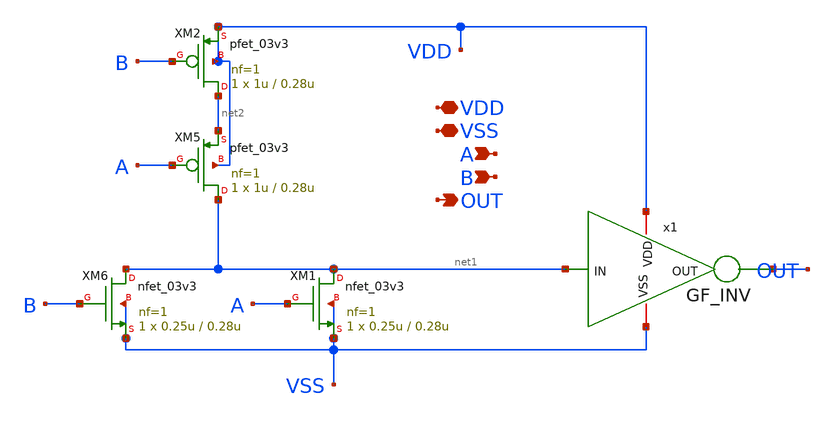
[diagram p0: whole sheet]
** sch_path: DAC_PAKISTAN_01/Pakistan1_Xschem/OR.sch
**.subckt OR VDD VSS A B OUT
*.iopin VDD
*.iopin VSS
*.ipin A
*.ipin B
*.opin OUT
x1 VSS VDD OUT net1 GF_INV
XM1 net1 A VSS VSS nfet_03v3 L=0.28u W=0.25u nf=1 ad='int((nf+1)/2) * W/nf * 0.18u' as='int((nf+2)/2) * W/nf * 0.18u'
+ pd='2*int((nf+1)/2) * (W/nf + 0.18u)' ps='2*int((nf+2)/2) * (W/nf + 0.18u)' nrd='0.18u / W' nrs='0.18u / W'
+ sa=0 sb=0 sd=0 m=1
XM2 net2 B VDD VDD pfet_03v3 L=0.28u W=1u nf=1 ad='int((nf+1)/2) * W/nf * 0.18u' as='int((nf+2)/2) * W/nf * 0.18u'
+ pd='2*int((nf+1)/2) * (W/nf + 0.18u)' ps='2*int((nf+2)/2) * (W/nf + 0.18u)' nrd='0.18u / W' nrs='0.18u / W'
+ sa=0 sb=0 sd=0 m=1
XM5 net1 A net2 VDD pfet_03v3 L=0.28u W=1u nf=1 ad='int((nf+1)/2) * W/nf * 0.18u' as='int((nf+2)/2) * W/nf * 0.18u'
+ pd='2*int((nf+1)/2) * (W/nf + 0.18u)' ps='2*int((nf+2)/2) * (W/nf + 0.18u)' nrd='0.18u / W' nrs='0.18u / W'
+ sa=0 sb=0 sd=0 m=1
XM6 net1 B VSS VSS nfet_03v3 L=0.28u W=0.25u nf=1 ad='int((nf+1)/2) * W/nf * 0.18u' as='int((nf+2)/2) * W/nf * 0.18u'
+ pd='2*int((nf+1)/2) * (W/nf + 0.18u)' ps='2*int((nf+2)/2) * (W/nf + 0.18u)' nrd='0.18u / W' nrs='0.18u / W'
+ sa=0 sb=0 sd=0 m=1
**.ends

* expanding   symbol:  GF_INV.sym # of pins=4
** sym_path: GF_INV.sym
** sch_path: GF_INV.sch
.subckt GF_INV VSS VDD OUT IN
*.iopin VDD
*.iopin VSS
*.ipin IN
*.opin OUT
XM1 OUT IN VSS VSS nfet_03v3 L=0.28u W=0.25u nf=1 ad='int((nf+1)/2) * W/nf * 0.18u' as='int((nf+2)/2) * W/nf * 0.18u'
+ pd='2*int((nf+1)/2) * (W/nf + 0.18u)' ps='2*int((nf+2)/2) * (W/nf + 0.18u)' nrd='0.18u / W' nrs='0.18u / W'
+ sa=0 sb=0 sd=0 m=1
XM2 OUT IN VDD VDD pfet_03v3 L=0.28u W=0.5u nf=1 ad='int((nf+1)/2) * W/nf * 0.18u' as='int((nf+2)/2) * W/nf * 0.18u'
+ pd='2*int((nf+1)/2) * (W/nf + 0.18u)' ps='2*int((nf+2)/2) * (W/nf + 0.18u)' nrd='0.18u / W' nrs='0.18u / W'
+ sa=0 sb=0 sd=0 m=1
.ends

.end
